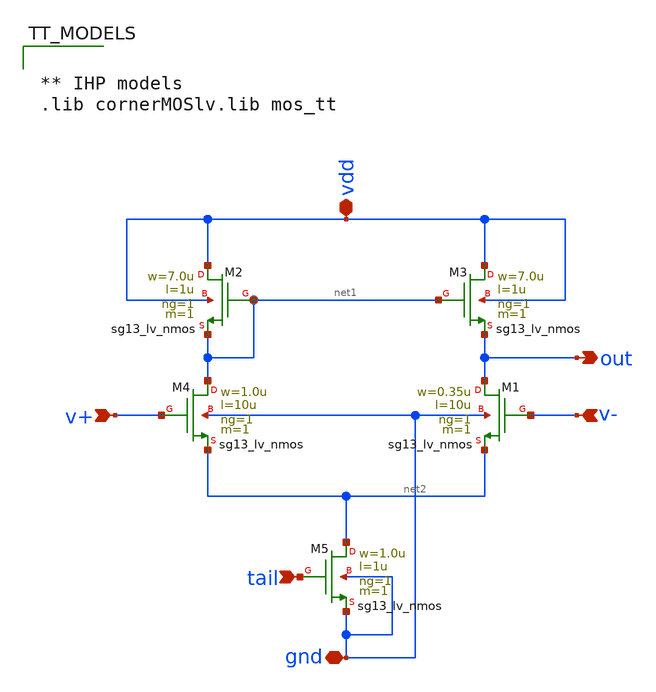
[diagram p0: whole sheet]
** sch_path: TempSensor/design_data/xschem/diff_amp.sch
**.subckt diff_amp v+ out v- tail gnd vdd
*.ipin v+
*.opin out
*.ipin v-
*.ipin tail
*.iopin gnd
*.iopin vdd
XM2 vdd net1 net1 vdd sg13_lv_nmos w=7.0u l=1u ng=1 m=1 mm_ok=1
XM1 out v- net2 gnd sg13_lv_nmos w=0.35u l=10u ng=1 m=1 mm_ok=1
XM3 vdd net1 out vdd sg13_lv_nmos w=7.0u l=1u ng=1 m=1 mm_ok=1
XM4 net1 v+ net2 gnd sg13_lv_nmos w=1.0u l=10u ng=1 m=1 mm_ok=1
XM5 net2 tail gnd gnd sg13_lv_nmos w=1.0u l=1u ng=1 m=1 mm_ok=1
**** begin user architecture code


** IHP models
.lib cornerMOSlv.lib mos_tt


**** end user architecture code
**.ends
.end
